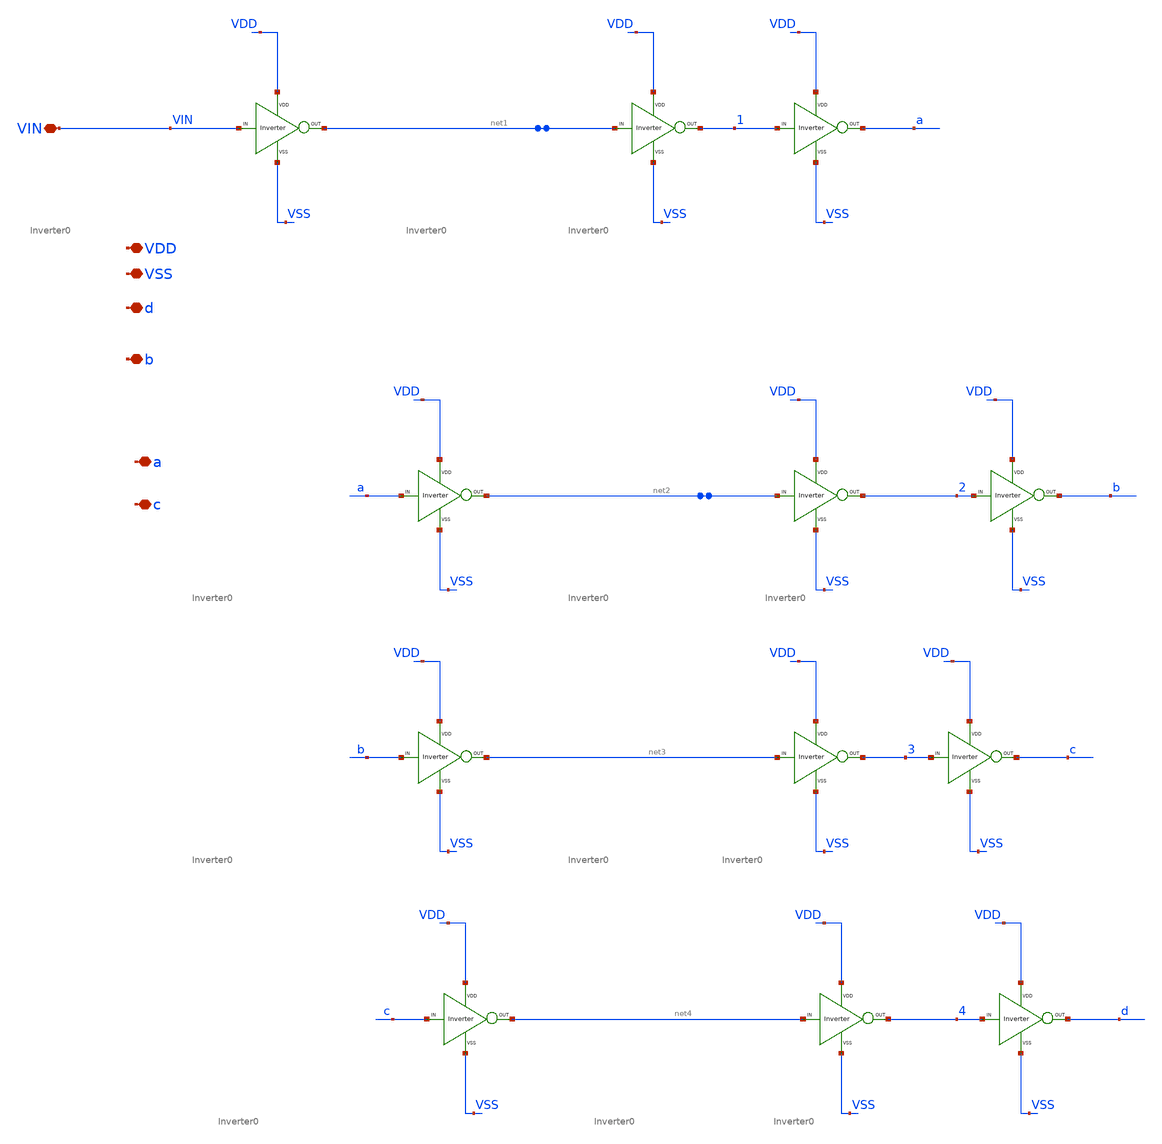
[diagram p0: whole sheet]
** sch_path: xschem/DC_DC_Converter_xschem/DC_DC_Converter/Delay_block_revised/delay1_sch.sch
**.subckt delay1_sch VDD VSS VIN d b a c
*.iopin VDD
*.iopin VSS
*.iopin VIN
*.iopin d
*.iopin b
*.iopin a
*.iopin c
X13 c net4 VDD VSS Inverter0
X11 4 d VDD VSS Inverter0
X7 b net3 VDD VSS Inverter0
X9 3 c VDD VSS Inverter0
X4 a net2 VDD VSS Inverter0
X6 2 b VDD VSS Inverter0
X1 VIN net1 VDD VSS Inverter0
X3 1 a VDD VSS Inverter0
X25 net1 1 VDD VSS Inverter0
X26 net2 2 VDD VSS Inverter0
X27 net3 3 VDD VSS Inverter0
X28 net4 4 VDD VSS Inverter0
**.ends

* expanding   symbol:  DC_DC_Converter/Delay_block_revised/Inverter_0/Inverter0.sym # of pins=4
** sym_path: xschem/DC_DC_Converter_xschem/DC_DC_Converter/Delay_block_revised/Inverter_0/Inverter0.sym
** sch_path: xschem/DC_DC_Converter_xschem/DC_DC_Converter/Delay_block_revised/Inverter_0/Inverter0.sch
.subckt Inverter0 VIN VOUT VDD VSS
*.ipin VIN
*.iopin VDD
*.iopin VSS
*.opin VOUT
XM1 VOUT VIN VSS VSS sky130_fd_pr__nfet_01v8 L=0.15 W=0.4 nf=1 ad='int((nf+1)/2) * W/nf * 0.29' as='int((nf+2)/2) * W/nf * 0.29'
+ pd='2*int((nf+1)/2) * (W/nf + 0.29)' ps='2*int((nf+2)/2) * (W/nf + 0.29)' nrd='0.29 / W' nrs='0.29 / W'
+ sa=0 sb=0 sd=0 mult=1 m=1
XM2 VOUT VIN VDD VDD sky130_fd_pr__pfet_01v8 L=0.15 W=1.2 nf=1 ad='int((nf+1)/2) * W/nf * 0.29' as='int((nf+2)/2) * W/nf * 0.29'
+ pd='2*int((nf+1)/2) * (W/nf + 0.29)' ps='2*int((nf+2)/2) * (W/nf + 0.29)' nrd='0.29 / W' nrs='0.29 / W'
+ sa=0 sb=0 sd=0 mult=1 m=1
.ends

.end
